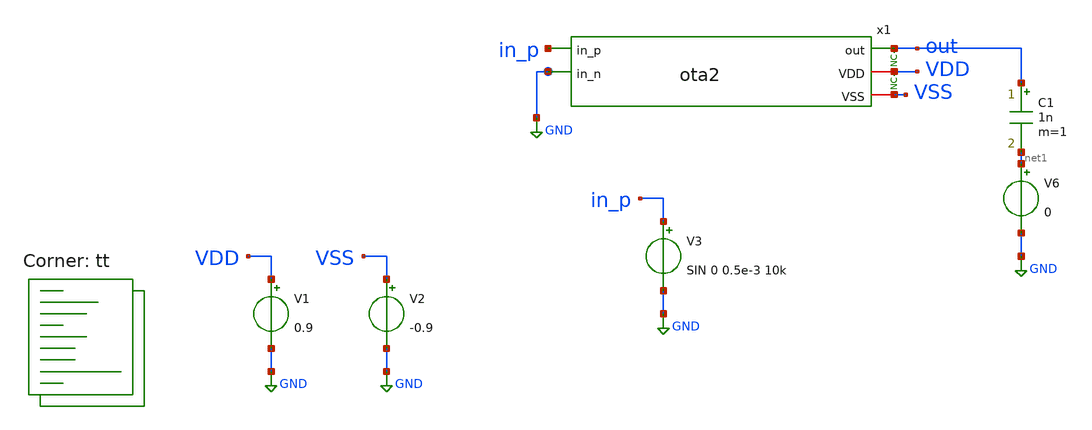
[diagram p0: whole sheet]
** sch_path: xschem/tests/ota2/ota2_integrator_test.sch
**.subckt ota2_integrator_test
V1 VDD GND 0.9
V2 VSS GND -0.9
V3 in_p GND SIN 0 0.5e-3 10k
* noconn VDD
* noconn out
x1 out in_p GND VDD VSS ota2
V6 net1 GND 0
C1 out net1 1n m=1
**** begin user architecture code
.lib $::SKYWATER_MODELS/sky130.lib.spice tt
 *.lib $::SKYWATER_MODELS/sky130.lib.spice tt
.include $::SKYWATER_STDCELLS/sky130_fd_sc_hd.spice




* ngspice commands
* ngspice commands
.options list act
.options method=gear
.temp 25

.control
save all
tran 1u 300u
plot out in_p
plot i(v6)

meas tran outptp pp v(out) from=0s to=300us
meas tran outmean avg v(out) from=0s to=300us

let gain = 20*log10($&outptp/0.002)
echo gain = $&gain

write ota2_test.raw
.endc



**** end user architecture code
**.ends
.GLOBAL GND
.end
